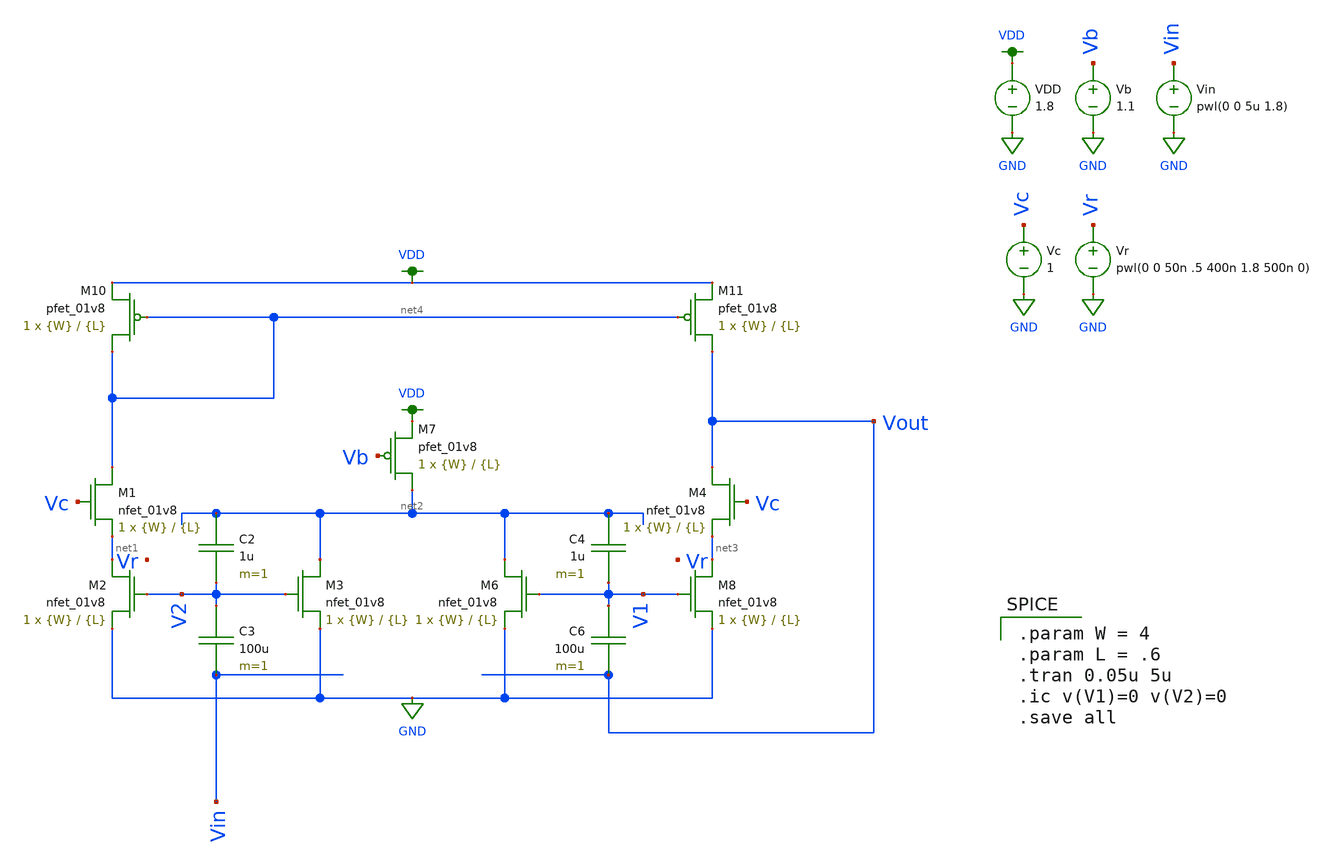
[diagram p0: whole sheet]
** sch_path: schematics/5_FGOP.sch
**.subckt 5_FGOP
XM1 net4 Vc net1 GND sky130_fd_pr__nfet_01v8 L={L} W={W} nf=1 ad='int((nf+1)/2) * W/nf * 0.29' as='int((nf+2)/2) * W/nf * 0.29'
+ pd='2*int((nf+1)/2) * (W/nf + 0.29)' ps='2*int((nf+2)/2) * (W/nf + 0.29)' nrd='0.29 / W' nrs='0.29 / W'
+ sa=0 sb=0 sd=0 mult=1 m=1
XM2 net1 V2 GND GND sky130_fd_pr__nfet_01v8 L={L} W={W} nf=1 ad='int((nf+1)/2) * W/nf * 0.29' as='int((nf+2)/2) * W/nf * 0.29'
+ pd='2*int((nf+1)/2) * (W/nf + 0.29)' ps='2*int((nf+2)/2) * (W/nf + 0.29)' nrd='0.29 / W' nrs='0.29 / W'
+ sa=0 sb=0 sd=0 mult=1 m=1
C2 net2 V2 1u m=1
C3 V2 Vin 100u m=1
XM3 net2 V2 GND GND sky130_fd_pr__nfet_01v8 L={L} W={W} nf=1 ad='int((nf+1)/2) * W/nf * 0.29' as='int((nf+2)/2) * W/nf * 0.29'
+ pd='2*int((nf+1)/2) * (W/nf + 0.29)' ps='2*int((nf+2)/2) * (W/nf + 0.29)' nrd='0.29 / W' nrs='0.29 / W'
+ sa=0 sb=0 sd=0 mult=1 m=1
XM4 Vout Vc net3 GND sky130_fd_pr__nfet_01v8 L={L} W={W} nf=1 ad='int((nf+1)/2) * W/nf * 0.29' as='int((nf+2)/2) * W/nf * 0.29'
+ pd='2*int((nf+1)/2) * (W/nf + 0.29)' ps='2*int((nf+2)/2) * (W/nf + 0.29)' nrd='0.29 / W' nrs='0.29 / W'
+ sa=0 sb=0 sd=0 mult=1 m=1
C4 net2 V1 1u m=1
C6 V1 Vout 100u m=1
XM6 net2 V1 GND GND sky130_fd_pr__nfet_01v8 L={L} W={W} nf=1 ad='int((nf+1)/2) * W/nf * 0.29' as='int((nf+2)/2) * W/nf * 0.29'
+ pd='2*int((nf+1)/2) * (W/nf + 0.29)' ps='2*int((nf+2)/2) * (W/nf + 0.29)' nrd='0.29 / W' nrs='0.29 / W'
+ sa=0 sb=0 sd=0 mult=1 m=1
XM7 net2 Vb VDD VDD sky130_fd_pr__pfet_01v8 L={L} W={W} nf=1 ad='int((nf+1)/2) * W/nf * 0.29' as='int((nf+2)/2) * W/nf * 0.29'
+ pd='2*int((nf+1)/2) * (W/nf + 0.29)' ps='2*int((nf+2)/2) * (W/nf + 0.29)' nrd='0.29 / W' nrs='0.29 / W'
+ sa=0 sb=0 sd=0 mult=1 m=1
VDD VDD GND 1.8
Vb Vb GND 1.1
Vc Vc GND 1
Vr Vr GND pwl(0 0 50n .5 400n 1.8 500n 0)
XM10 net4 net4 VDD VDD sky130_fd_pr__pfet_01v8 L={L} W={W} nf=1 ad='int((nf+1)/2) * W/nf * 0.29' as='int((nf+2)/2) * W/nf * 0.29'
+ pd='2*int((nf+1)/2) * (W/nf + 0.29)' ps='2*int((nf+2)/2) * (W/nf + 0.29)' nrd='0.29 / W' nrs='0.29 / W'
+ sa=0 sb=0 sd=0 mult=1 m=1
XM11 Vout net4 VDD VDD sky130_fd_pr__pfet_01v8 L={L} W={W} nf=1 ad='int((nf+1)/2) * W/nf * 0.29' as='int((nf+2)/2) * W/nf * 0.29'
+ pd='2*int((nf+1)/2) * (W/nf + 0.29)' ps='2*int((nf+2)/2) * (W/nf + 0.29)' nrd='0.29 / W' nrs='0.29 / W'
+ sa=0 sb=0 sd=0 mult=1 m=1
Vin Vin GND pwl(0 0 5u 1.8)
XM8 net3 V1 GND GND sky130_fd_pr__nfet_01v8 L={L} W={W} nf=1 ad='int((nf+1)/2) * W/nf * 0.29' as='int((nf+2)/2) * W/nf * 0.29'
+ pd='2*int((nf+1)/2) * (W/nf + 0.29)' ps='2*int((nf+2)/2) * (W/nf + 0.29)' nrd='0.29 / W' nrs='0.29 / W'
+ sa=0 sb=0 sd=0 mult=1 m=1
**** begin user architecture code

.param W = 4
.param L = .6
.tran 0.05u 5u
.ic v(V1)=0 v(V2)=0
.save all


.option wnflag=1
.param MC_SWITCH=0.0
.lib ~/skywater/skywater-pdk/libraries/sky130_fd_pr_ngspice/latest/models/sky130.lib.spice tt

**** end user architecture code
**.ends
.GLOBAL GND
.GLOBAL VDD
.end
